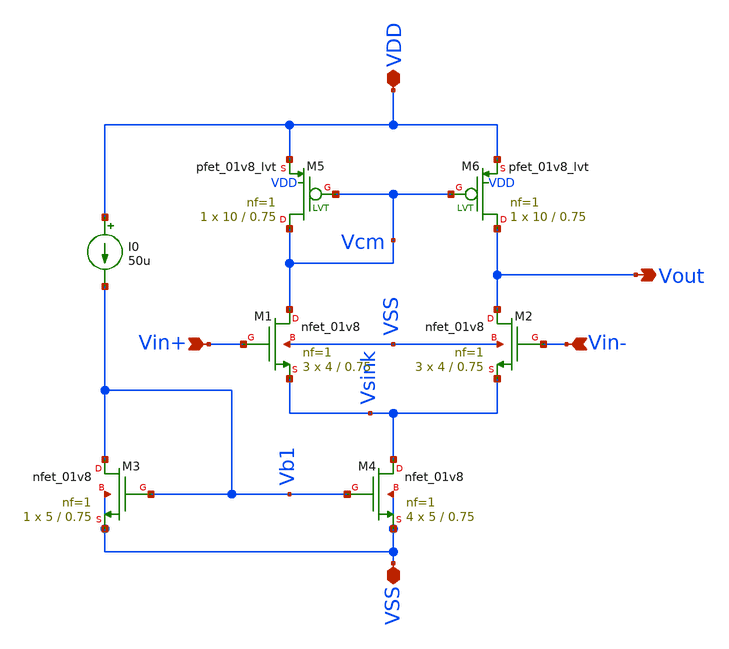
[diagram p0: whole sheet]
** sch_path: xschem/Amplifiers/5TOpamp.sch
**.subckt 5TOpamp VDD VSS Vin- Vin+ Vout
*.iopin VDD
*.iopin VSS
*.ipin Vin-
*.ipin Vin+
*.opin Vout
I0 VDD Vb1 50u
XM1 Vcm Vin+ Vsink VSS sky130_fd_pr__nfet_01v8 L=0.75 W=4 nf=1 ad='int((nf+1)/2) * W/nf * 0.29' as='int((nf+2)/2) * W/nf * 0.29'
+ pd='2*int((nf+1)/2) * (W/nf + 0.29)' ps='2*int((nf+2)/2) * (W/nf + 0.29)' nrd='0.29 / W' nrs='0.29 / W'
+ sa=0 sb=0 sd=0 mult=3 m=3
XM2 Vout Vin- Vsink VSS sky130_fd_pr__nfet_01v8 L=0.75 W=4 nf=1 ad='int((nf+1)/2) * W/nf * 0.29' as='int((nf+2)/2) * W/nf * 0.29'
+ pd='2*int((nf+1)/2) * (W/nf + 0.29)' ps='2*int((nf+2)/2) * (W/nf + 0.29)' nrd='0.29 / W' nrs='0.29 / W'
+ sa=0 sb=0 sd=0 mult=3 m=3
XM3 Vb1 Vb1 VSS VSS sky130_fd_pr__nfet_01v8 L=0.75 W=5 nf=1 ad='int((nf+1)/2) * W/nf * 0.29' as='int((nf+2)/2) * W/nf * 0.29'
+ pd='2*int((nf+1)/2) * (W/nf + 0.29)' ps='2*int((nf+2)/2) * (W/nf + 0.29)' nrd='0.29 / W' nrs='0.29 / W'
+ sa=0 sb=0 sd=0 mult=1 m=1
XM4 Vsink Vb1 VSS VSS sky130_fd_pr__nfet_01v8 L=0.75 W=5 nf=1 ad='int((nf+1)/2) * W/nf * 0.29' as='int((nf+2)/2) * W/nf * 0.29'
+ pd='2*int((nf+1)/2) * (W/nf + 0.29)' ps='2*int((nf+2)/2) * (W/nf + 0.29)' nrd='0.29 / W' nrs='0.29 / W'
+ sa=0 sb=0 sd=0 mult=4 m=4
XM5 Vcm Vcm VDD VDD sky130_fd_pr__pfet_01v8_lvt L=0.75 W=10 nf=1 ad='int((nf+1)/2) * W/nf * 0.29' as='int((nf+2)/2) * W/nf * 0.29'
+ pd='2*int((nf+1)/2) * (W/nf + 0.29)' ps='2*int((nf+2)/2) * (W/nf + 0.29)' nrd='0.29 / W' nrs='0.29 / W'
+ sa=0 sb=0 sd=0 mult=1 m=1
XM6 Vout Vcm VDD VDD sky130_fd_pr__pfet_01v8_lvt L=0.75 W=10 nf=1 ad='int((nf+1)/2) * W/nf * 0.29' as='int((nf+2)/2) * W/nf * 0.29'
+ pd='2*int((nf+1)/2) * (W/nf + 0.29)' ps='2*int((nf+2)/2) * (W/nf + 0.29)' nrd='0.29 / W' nrs='0.29 / W'
+ sa=0 sb=0 sd=0 mult=1 m=1
**.ends
.end
